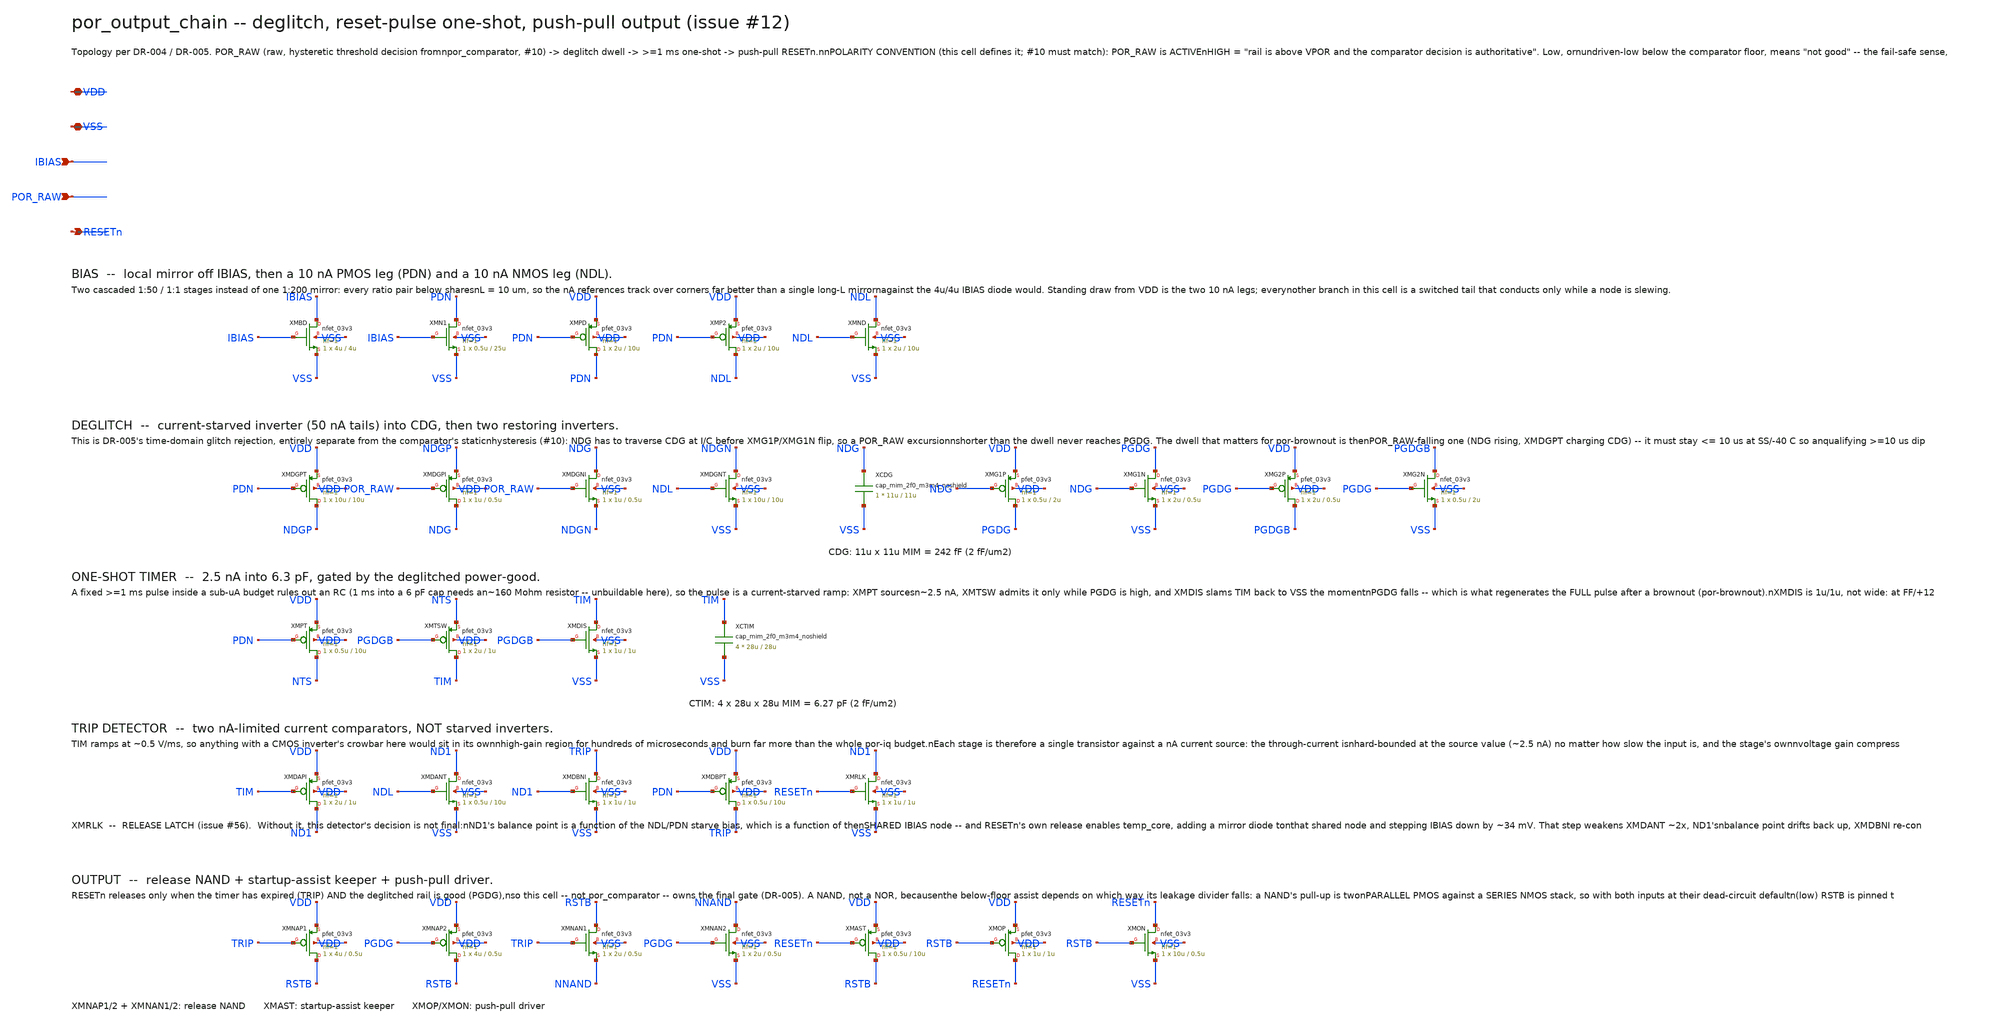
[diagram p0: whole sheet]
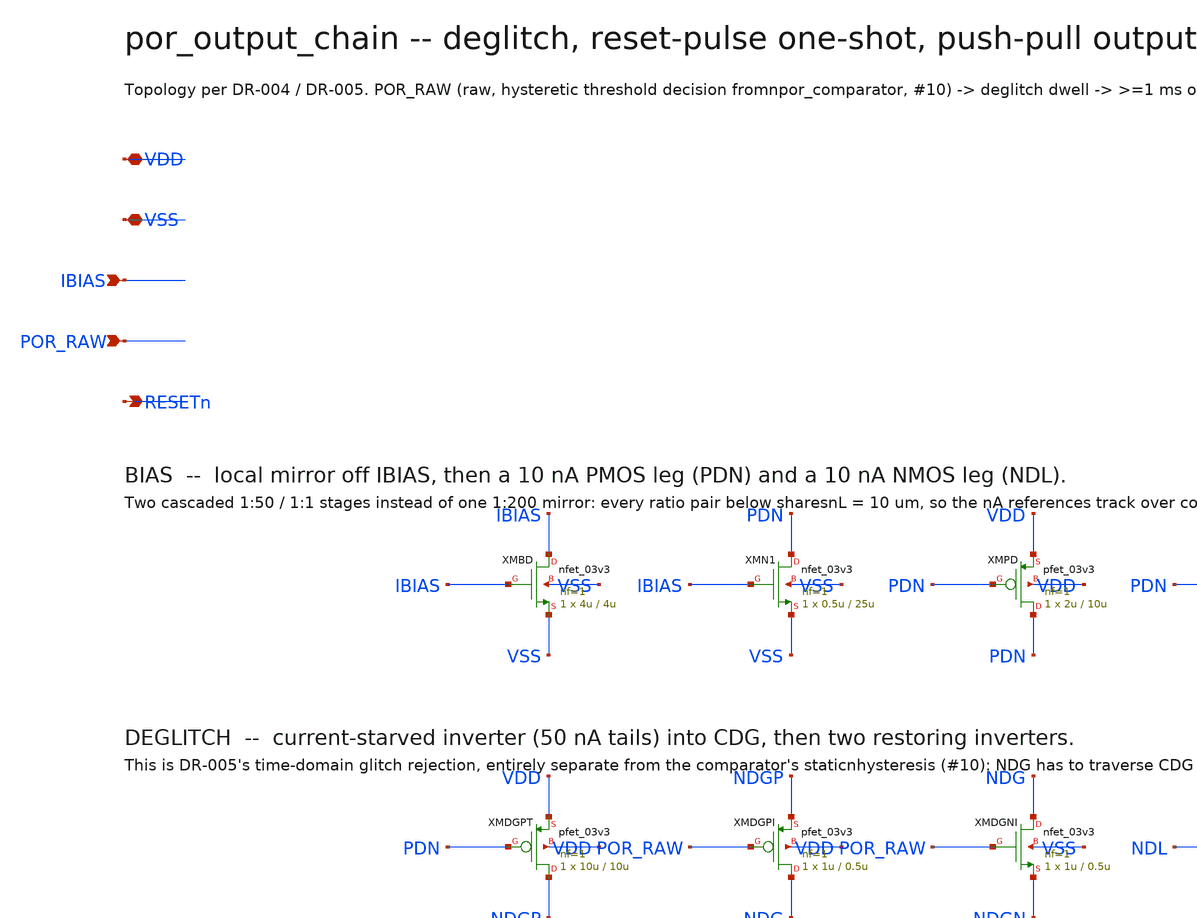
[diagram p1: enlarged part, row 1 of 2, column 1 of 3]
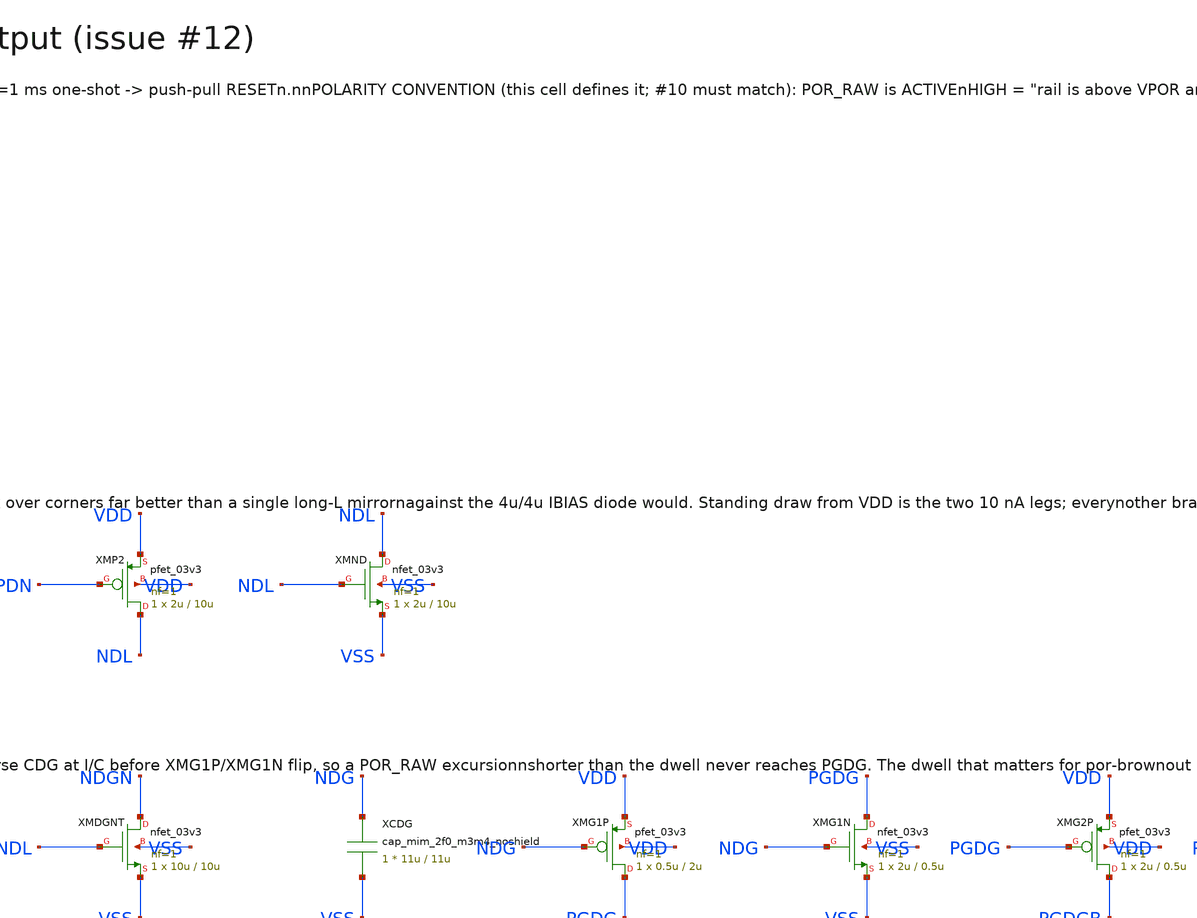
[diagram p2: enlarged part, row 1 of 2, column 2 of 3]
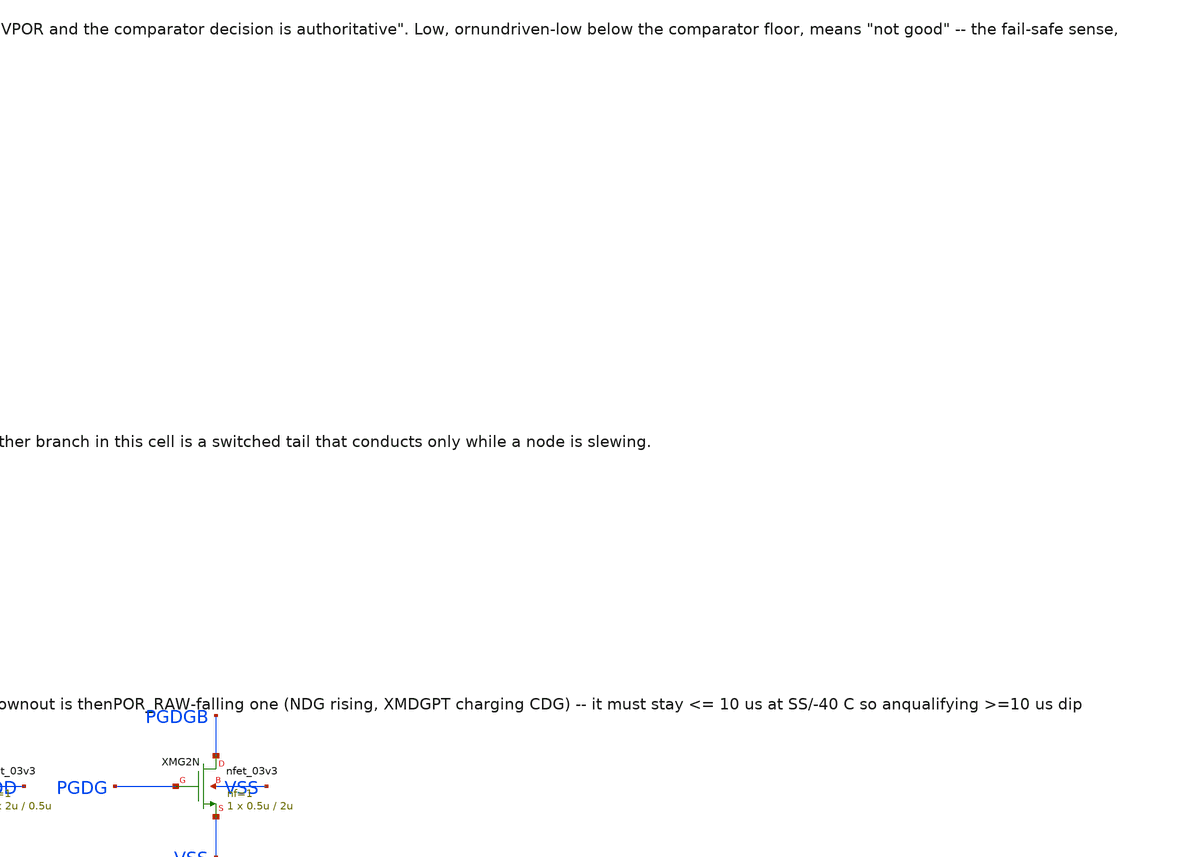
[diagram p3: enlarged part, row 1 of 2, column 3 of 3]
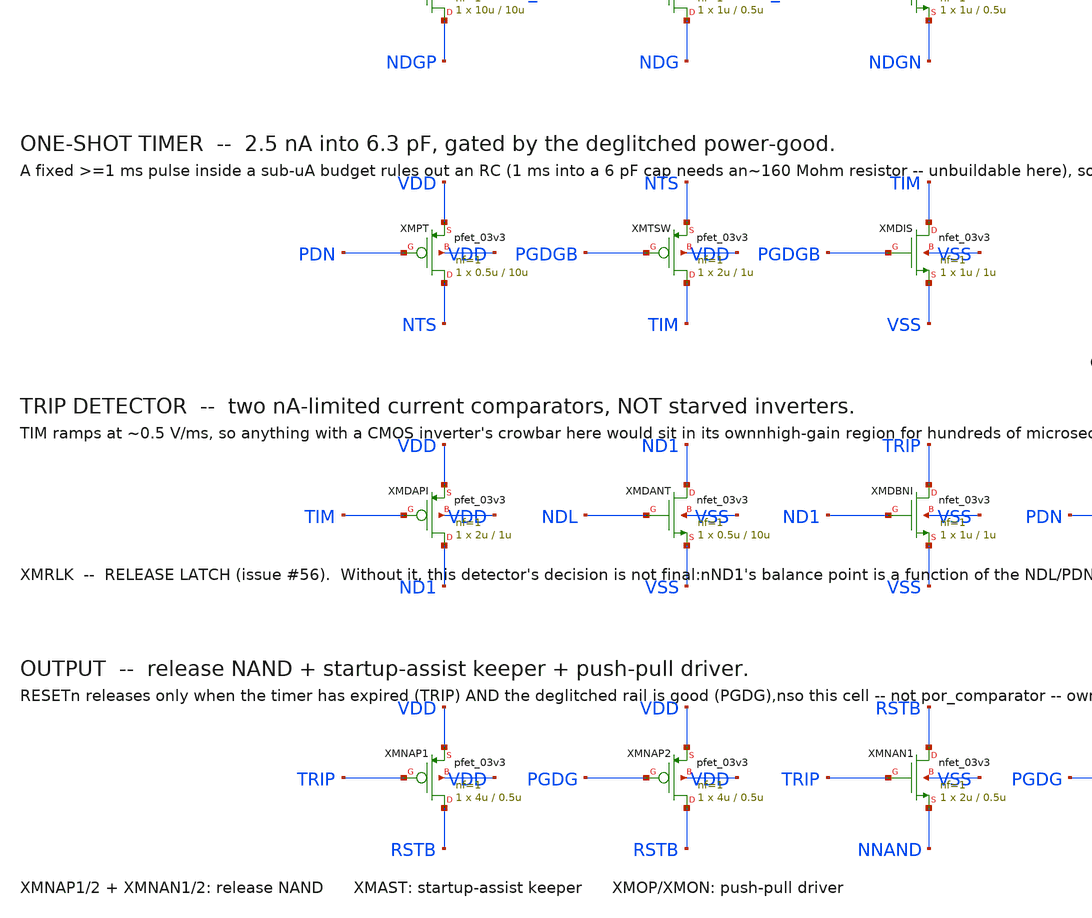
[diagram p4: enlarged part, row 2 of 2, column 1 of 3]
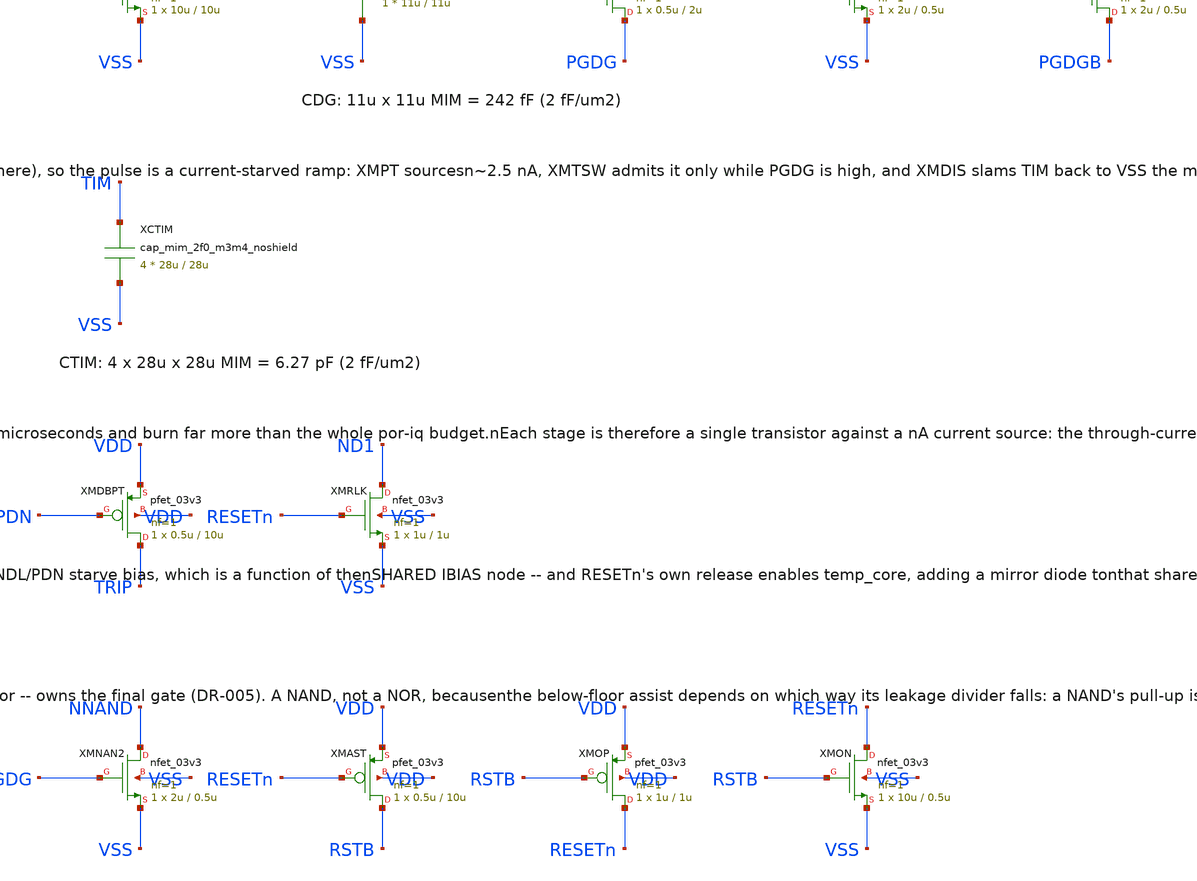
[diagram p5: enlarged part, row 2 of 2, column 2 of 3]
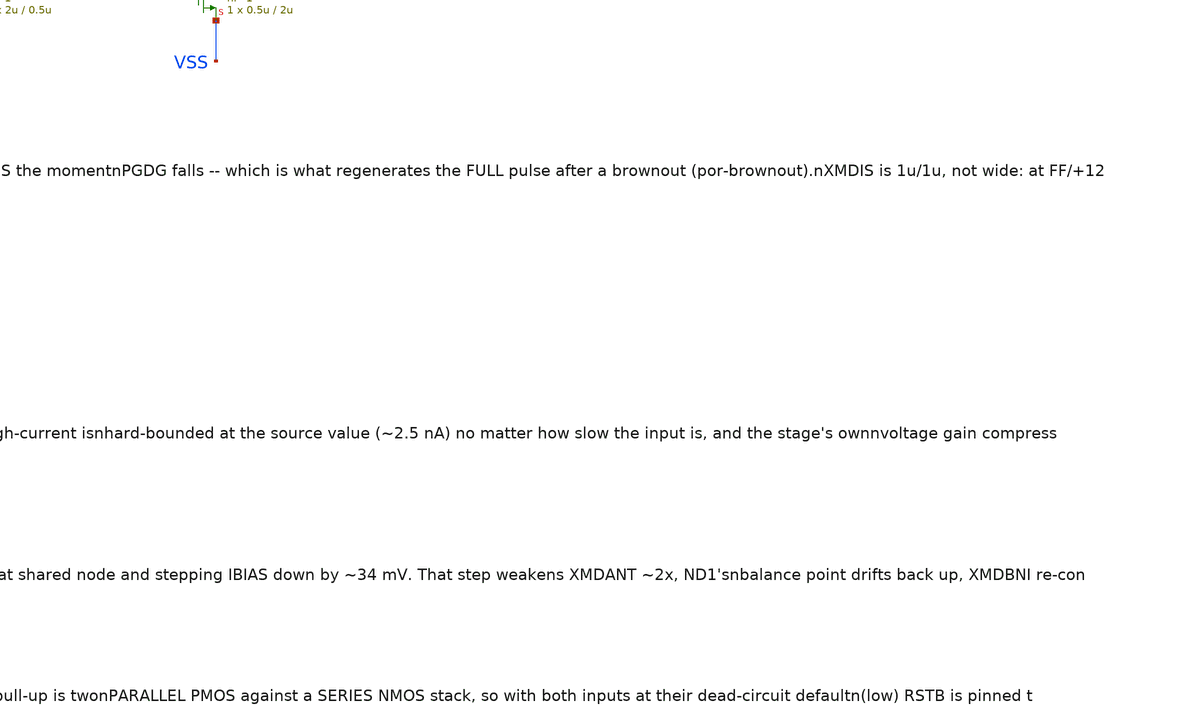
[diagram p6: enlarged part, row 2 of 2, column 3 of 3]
** sch_path: design/por_output_chain.sch
**.subckt por_output_chain VDD VSS IBIAS POR_RAW RESETn
*.iopin VDD
*.iopin VSS
*.ipin IBIAS
*.ipin POR_RAW
*.opin RESETn
XMBD IBIAS IBIAS VSS VSS nfet_03v3 L=4u W=4u nf=1 ad='int((nf+1)/2) * W/nf * 0.18u' as='int((nf+2)/2) * W/nf * 0.18u'
+ pd='2*int((nf+1)/2) * (W/nf + 0.18u)' ps='2*int((nf+2)/2) * (W/nf + 0.18u)' nrd='0.18u / W' nrs='0.18u / W'
+ sa=0 sb=0 sd=0 m=1
XMN1 PDN IBIAS VSS VSS nfet_03v3 L=25u W=0.5u nf=1 ad='int((nf+1)/2) * W/nf * 0.18u' as='int((nf+2)/2) * W/nf * 0.18u'
+ pd='2*int((nf+1)/2) * (W/nf + 0.18u)' ps='2*int((nf+2)/2) * (W/nf + 0.18u)' nrd='0.18u / W' nrs='0.18u / W'
+ sa=0 sb=0 sd=0 m=1
XMPD PDN PDN VDD VDD pfet_03v3 L=10u W=2u nf=1 ad='int((nf+1)/2) * W/nf * 0.18u' as='int((nf+2)/2) * W/nf * 0.18u'
+ pd='2*int((nf+1)/2) * (W/nf + 0.18u)' ps='2*int((nf+2)/2) * (W/nf + 0.18u)' nrd='0.18u / W' nrs='0.18u / W'
+ sa=0 sb=0 sd=0 m=1
XMP2 NDL PDN VDD VDD pfet_03v3 L=10u W=2u nf=1 ad='int((nf+1)/2) * W/nf * 0.18u' as='int((nf+2)/2) * W/nf * 0.18u'
+ pd='2*int((nf+1)/2) * (W/nf + 0.18u)' ps='2*int((nf+2)/2) * (W/nf + 0.18u)' nrd='0.18u / W' nrs='0.18u / W'
+ sa=0 sb=0 sd=0 m=1
XMND NDL NDL VSS VSS nfet_03v3 L=10u W=2u nf=1 ad='int((nf+1)/2) * W/nf * 0.18u' as='int((nf+2)/2) * W/nf * 0.18u'
+ pd='2*int((nf+1)/2) * (W/nf + 0.18u)' ps='2*int((nf+2)/2) * (W/nf + 0.18u)' nrd='0.18u / W' nrs='0.18u / W'
+ sa=0 sb=0 sd=0 m=1
XMDGPT NDGP PDN VDD VDD pfet_03v3 L=10u W=10u nf=1 ad='int((nf+1)/2) * W/nf * 0.18u' as='int((nf+2)/2) * W/nf * 0.18u'
+ pd='2*int((nf+1)/2) * (W/nf + 0.18u)' ps='2*int((nf+2)/2) * (W/nf + 0.18u)' nrd='0.18u / W' nrs='0.18u / W'
+ sa=0 sb=0 sd=0 m=1
XMDGPI NDG POR_RAW NDGP VDD pfet_03v3 L=0.5u W=1u nf=1 ad='int((nf+1)/2) * W/nf * 0.18u' as='int((nf+2)/2) * W/nf * 0.18u'
+ pd='2*int((nf+1)/2) * (W/nf + 0.18u)' ps='2*int((nf+2)/2) * (W/nf + 0.18u)' nrd='0.18u / W' nrs='0.18u / W'
+ sa=0 sb=0 sd=0 m=1
XMDGNI NDG POR_RAW NDGN VSS nfet_03v3 L=0.5u W=1u nf=1 ad='int((nf+1)/2) * W/nf * 0.18u' as='int((nf+2)/2) * W/nf * 0.18u'
+ pd='2*int((nf+1)/2) * (W/nf + 0.18u)' ps='2*int((nf+2)/2) * (W/nf + 0.18u)' nrd='0.18u / W' nrs='0.18u / W'
+ sa=0 sb=0 sd=0 m=1
XMDGNT NDGN NDL VSS VSS nfet_03v3 L=10u W=10u nf=1 ad='int((nf+1)/2) * W/nf * 0.18u' as='int((nf+2)/2) * W/nf * 0.18u'
+ pd='2*int((nf+1)/2) * (W/nf + 0.18u)' ps='2*int((nf+2)/2) * (W/nf + 0.18u)' nrd='0.18u / W' nrs='0.18u / W'
+ sa=0 sb=0 sd=0 m=1
XCDG NDG VSS cap_mim_2f0_m3m4_noshield c_width=11u c_length=11u m=1
XMG1P PGDG NDG VDD VDD pfet_03v3 L=2u W=0.5u nf=1 ad='int((nf+1)/2) * W/nf * 0.18u' as='int((nf+2)/2) * W/nf * 0.18u'
+ pd='2*int((nf+1)/2) * (W/nf + 0.18u)' ps='2*int((nf+2)/2) * (W/nf + 0.18u)' nrd='0.18u / W' nrs='0.18u / W'
+ sa=0 sb=0 sd=0 m=1
XMG1N PGDG NDG VSS VSS nfet_03v3 L=0.5u W=2u nf=1 ad='int((nf+1)/2) * W/nf * 0.18u' as='int((nf+2)/2) * W/nf * 0.18u'
+ pd='2*int((nf+1)/2) * (W/nf + 0.18u)' ps='2*int((nf+2)/2) * (W/nf + 0.18u)' nrd='0.18u / W' nrs='0.18u / W'
+ sa=0 sb=0 sd=0 m=1
XMG2P PGDGB PGDG VDD VDD pfet_03v3 L=0.5u W=2u nf=1 ad='int((nf+1)/2) * W/nf * 0.18u' as='int((nf+2)/2) * W/nf * 0.18u'
+ pd='2*int((nf+1)/2) * (W/nf + 0.18u)' ps='2*int((nf+2)/2) * (W/nf + 0.18u)' nrd='0.18u / W' nrs='0.18u / W'
+ sa=0 sb=0 sd=0 m=1
XMG2N PGDGB PGDG VSS VSS nfet_03v3 L=2u W=0.5u nf=1 ad='int((nf+1)/2) * W/nf * 0.18u' as='int((nf+2)/2) * W/nf * 0.18u'
+ pd='2*int((nf+1)/2) * (W/nf + 0.18u)' ps='2*int((nf+2)/2) * (W/nf + 0.18u)' nrd='0.18u / W' nrs='0.18u / W'
+ sa=0 sb=0 sd=0 m=1
XMPT NTS PDN VDD VDD pfet_03v3 L=10u W=0.5u nf=1 ad='int((nf+1)/2) * W/nf * 0.18u' as='int((nf+2)/2) * W/nf * 0.18u'
+ pd='2*int((nf+1)/2) * (W/nf + 0.18u)' ps='2*int((nf+2)/2) * (W/nf + 0.18u)' nrd='0.18u / W' nrs='0.18u / W'
+ sa=0 sb=0 sd=0 m=1
XMTSW TIM PGDGB NTS VDD pfet_03v3 L=1u W=2u nf=1 ad='int((nf+1)/2) * W/nf * 0.18u' as='int((nf+2)/2) * W/nf * 0.18u'
+ pd='2*int((nf+1)/2) * (W/nf + 0.18u)' ps='2*int((nf+2)/2) * (W/nf + 0.18u)' nrd='0.18u / W' nrs='0.18u / W'
+ sa=0 sb=0 sd=0 m=1
XMDIS TIM PGDGB VSS VSS nfet_03v3 L=1u W=1u nf=1 ad='int((nf+1)/2) * W/nf * 0.18u' as='int((nf+2)/2) * W/nf * 0.18u'
+ pd='2*int((nf+1)/2) * (W/nf + 0.18u)' ps='2*int((nf+2)/2) * (W/nf + 0.18u)' nrd='0.18u / W' nrs='0.18u / W'
+ sa=0 sb=0 sd=0 m=1
XCTIM TIM VSS cap_mim_2f0_m3m4_noshield c_width=28u c_length=28u m=4
XMDAPI ND1 TIM VDD VDD pfet_03v3 L=1u W=2u nf=1 ad='int((nf+1)/2) * W/nf * 0.18u' as='int((nf+2)/2) * W/nf * 0.18u'
+ pd='2*int((nf+1)/2) * (W/nf + 0.18u)' ps='2*int((nf+2)/2) * (W/nf + 0.18u)' nrd='0.18u / W' nrs='0.18u / W'
+ sa=0 sb=0 sd=0 m=1
XMDANT ND1 NDL VSS VSS nfet_03v3 L=10u W=0.5u nf=1 ad='int((nf+1)/2) * W/nf * 0.18u' as='int((nf+2)/2) * W/nf * 0.18u'
+ pd='2*int((nf+1)/2) * (W/nf + 0.18u)' ps='2*int((nf+2)/2) * (W/nf + 0.18u)' nrd='0.18u / W' nrs='0.18u / W'
+ sa=0 sb=0 sd=0 m=1
XMDBNI TRIP ND1 VSS VSS nfet_03v3 L=1u W=1u nf=1 ad='int((nf+1)/2) * W/nf * 0.18u' as='int((nf+2)/2) * W/nf * 0.18u'
+ pd='2*int((nf+1)/2) * (W/nf + 0.18u)' ps='2*int((nf+2)/2) * (W/nf + 0.18u)' nrd='0.18u / W' nrs='0.18u / W'
+ sa=0 sb=0 sd=0 m=1
XMDBPT TRIP PDN VDD VDD pfet_03v3 L=10u W=0.5u nf=1 ad='int((nf+1)/2) * W/nf * 0.18u' as='int((nf+2)/2) * W/nf * 0.18u'
+ pd='2*int((nf+1)/2) * (W/nf + 0.18u)' ps='2*int((nf+2)/2) * (W/nf + 0.18u)' nrd='0.18u / W' nrs='0.18u / W'
+ sa=0 sb=0 sd=0 m=1
XMRLK ND1 RESETn VSS VSS nfet_03v3 L=1u W=1u nf=1 ad='int((nf+1)/2) * W/nf * 0.18u' as='int((nf+2)/2) * W/nf * 0.18u'
+ pd='2*int((nf+1)/2) * (W/nf + 0.18u)' ps='2*int((nf+2)/2) * (W/nf + 0.18u)' nrd='0.18u / W' nrs='0.18u / W'
+ sa=0 sb=0 sd=0 m=1
XMNAP1 RSTB TRIP VDD VDD pfet_03v3 L=0.5u W=4u nf=1 ad='int((nf+1)/2) * W/nf * 0.18u' as='int((nf+2)/2) * W/nf * 0.18u'
+ pd='2*int((nf+1)/2) * (W/nf + 0.18u)' ps='2*int((nf+2)/2) * (W/nf + 0.18u)' nrd='0.18u / W' nrs='0.18u / W'
+ sa=0 sb=0 sd=0 m=1
XMNAP2 RSTB PGDG VDD VDD pfet_03v3 L=0.5u W=4u nf=1 ad='int((nf+1)/2) * W/nf * 0.18u' as='int((nf+2)/2) * W/nf * 0.18u'
+ pd='2*int((nf+1)/2) * (W/nf + 0.18u)' ps='2*int((nf+2)/2) * (W/nf + 0.18u)' nrd='0.18u / W' nrs='0.18u / W'
+ sa=0 sb=0 sd=0 m=1
XMNAN1 RSTB TRIP NNAND VSS nfet_03v3 L=0.5u W=2u nf=1 ad='int((nf+1)/2) * W/nf * 0.18u' as='int((nf+2)/2) * W/nf * 0.18u'
+ pd='2*int((nf+1)/2) * (W/nf + 0.18u)' ps='2*int((nf+2)/2) * (W/nf + 0.18u)' nrd='0.18u / W' nrs='0.18u / W'
+ sa=0 sb=0 sd=0 m=1
XMNAN2 NNAND PGDG VSS VSS nfet_03v3 L=0.5u W=2u nf=1 ad='int((nf+1)/2) * W/nf * 0.18u' as='int((nf+2)/2) * W/nf * 0.18u'
+ pd='2*int((nf+1)/2) * (W/nf + 0.18u)' ps='2*int((nf+2)/2) * (W/nf + 0.18u)' nrd='0.18u / W' nrs='0.18u / W'
+ sa=0 sb=0 sd=0 m=1
XMAST RSTB RESETn VDD VDD pfet_03v3 L=10u W=0.5u nf=1 ad='int((nf+1)/2) * W/nf * 0.18u' as='int((nf+2)/2) * W/nf * 0.18u'
+ pd='2*int((nf+1)/2) * (W/nf + 0.18u)' ps='2*int((nf+2)/2) * (W/nf + 0.18u)' nrd='0.18u / W' nrs='0.18u / W'
+ sa=0 sb=0 sd=0 m=1
XMOP RESETn RSTB VDD VDD pfet_03v3 L=1u W=1u nf=1 ad='int((nf+1)/2) * W/nf * 0.18u' as='int((nf+2)/2) * W/nf * 0.18u'
+ pd='2*int((nf+1)/2) * (W/nf + 0.18u)' ps='2*int((nf+2)/2) * (W/nf + 0.18u)' nrd='0.18u / W' nrs='0.18u / W'
+ sa=0 sb=0 sd=0 m=1
XMON RESETn RSTB VSS VSS nfet_03v3 L=0.5u W=10u nf=1 ad='int((nf+1)/2) * W/nf * 0.18u' as='int((nf+2)/2) * W/nf * 0.18u'
+ pd='2*int((nf+1)/2) * (W/nf + 0.18u)' ps='2*int((nf+2)/2) * (W/nf + 0.18u)' nrd='0.18u / W' nrs='0.18u / W'
+ sa=0 sb=0 sd=0 m=1
**.ends
.end
